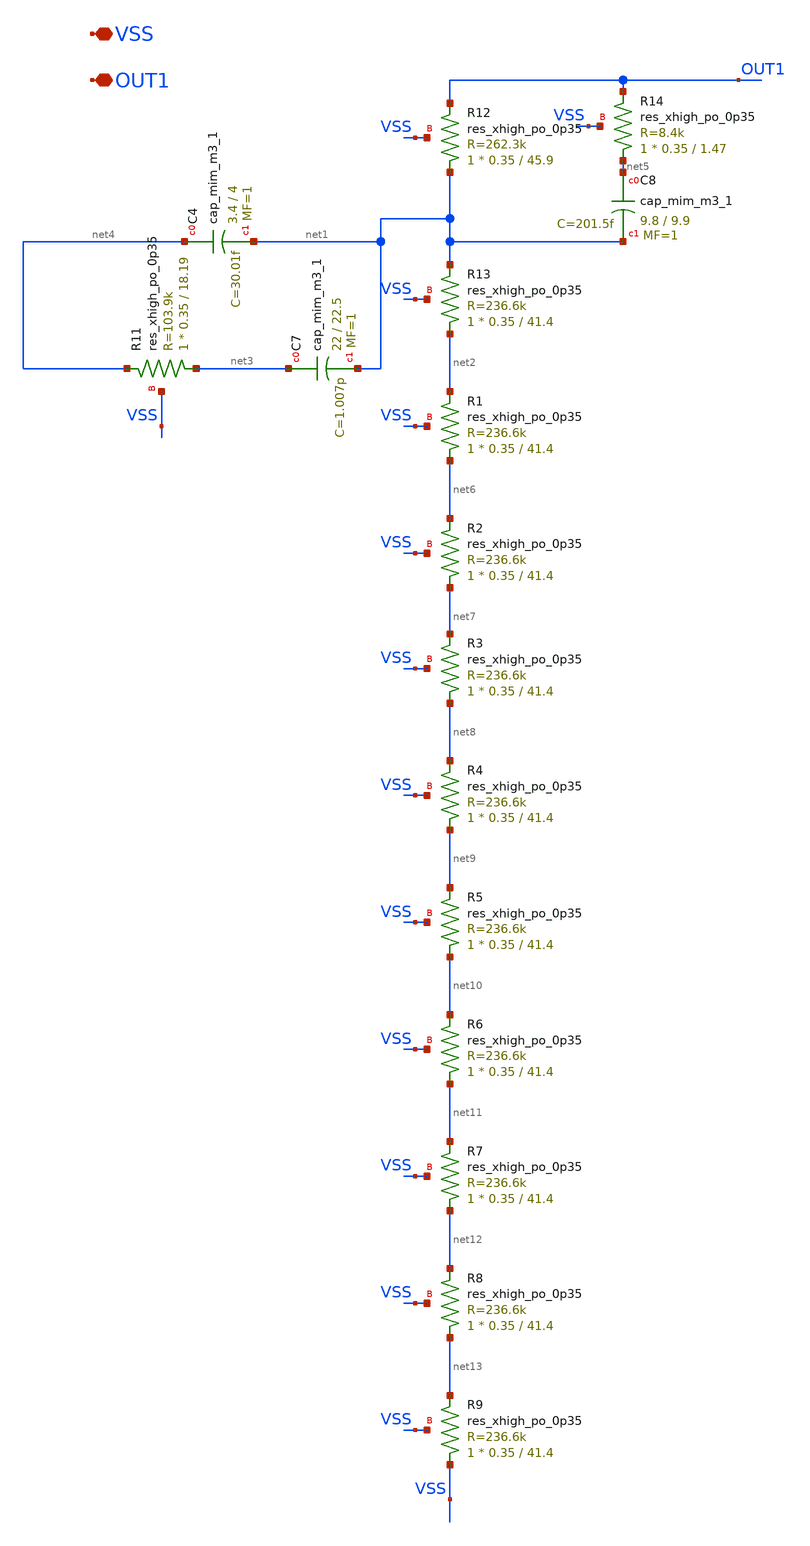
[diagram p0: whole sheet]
** sch_path: xschem/DC_DC_Converter_xschem/DC_DC_Converter/TOP_LEVEL/Top_Final/cap_res.sch
**.subckt cap_res VSS OUT1
*.iopin VSS
*.iopin OUT1
XC4 net4 net1 sky130_fd_pr__cap_mim_m3_1 W=3.4 L=4 MF=1 m=1
XC7 net3 net1 sky130_fd_pr__cap_mim_m3_1 W=22 L=22.5 MF=1 m=1
XC8 net5 net1 sky130_fd_pr__cap_mim_m3_1 W=9.8 L=9.9 MF=1 m=1
XR11 net3 net4 VSS sky130_fd_pr__res_xhigh_po_0p35 L=18.19 mult=1 m=1
XR12 net1 OUT1 VSS sky130_fd_pr__res_xhigh_po_0p35 L=45.9 mult=1 m=1
XR13 net2 net1 VSS sky130_fd_pr__res_xhigh_po_0p35 L=41.4 mult=1 m=1
XR14 net5 OUT1 VSS sky130_fd_pr__res_xhigh_po_0p35 L=1.47 mult=1 m=1
XR1 net6 net2 VSS sky130_fd_pr__res_xhigh_po_0p35 L=41.4 mult=1 m=1
XR2 net7 net6 VSS sky130_fd_pr__res_xhigh_po_0p35 L=41.4 mult=1 m=1
XR3 net8 net7 VSS sky130_fd_pr__res_xhigh_po_0p35 L=41.4 mult=1 m=1
XR4 net9 net8 VSS sky130_fd_pr__res_xhigh_po_0p35 L=41.4 mult=1 m=1
XR5 net10 net9 VSS sky130_fd_pr__res_xhigh_po_0p35 L=41.4 mult=1 m=1
XR6 net11 net10 VSS sky130_fd_pr__res_xhigh_po_0p35 L=41.4 mult=1 m=1
XR7 net12 net11 VSS sky130_fd_pr__res_xhigh_po_0p35 L=41.4 mult=1 m=1
XR8 net13 net12 VSS sky130_fd_pr__res_xhigh_po_0p35 L=41.4 mult=1 m=1
XR9 VSS net13 VSS sky130_fd_pr__res_xhigh_po_0p35 L=41.4 mult=1 m=1
**.ends
.end
